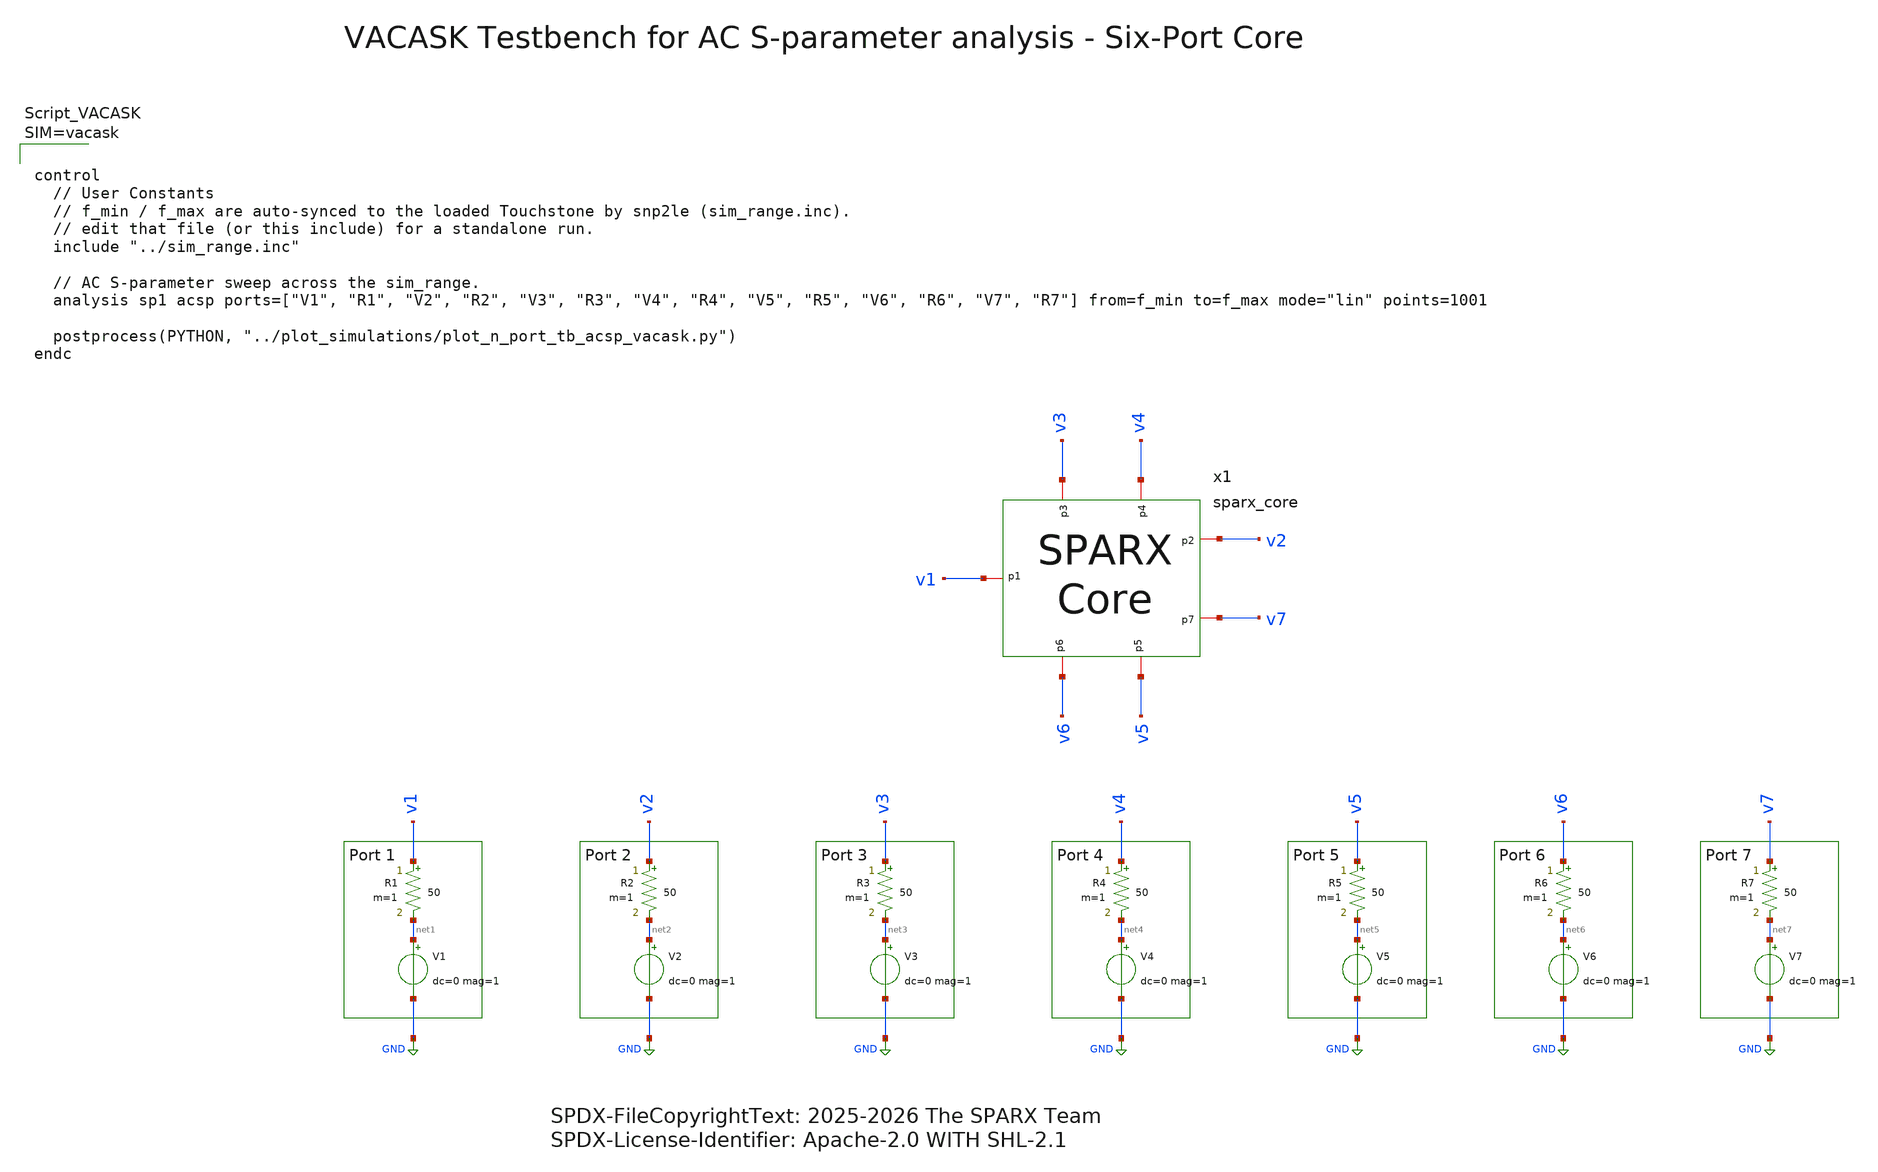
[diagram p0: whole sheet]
** sch_path: testbenches/xschem/sparx_core_tb_acsp_vacask.sch
* SPDX-FileCopyrightText: 2025-2026 The SPARX Team
* SPDX-License-Identifier: Apache-2.0 WITH SHL-2.1
**.subckt sparx_core_tb_acsp_vacask
R1 v1 net1 50 m=1
V1 net1 GND dc=0 mag=1
R2 v2 net2 50 m=1
V2 net2 GND dc=0 mag=1
R3 v3 net3 50 m=1
V3 net3 GND dc=0 mag=1
R4 v4 net4 50 m=1
V4 net4 GND dc=0 mag=1
R5 v5 net5 50 m=1
V5 net5 GND dc=0 mag=1
R6 v6 net6 50 m=1
V6 net6 GND dc=0 mag=1
R7 v7 net7 50 m=1
V7 net7 GND dc=0 mag=1
x1 v3 v4 v2 v1 v7 v5 v6 sparx_core
**** begin user architecture code






**** end user architecture code
**.ends

* expanding   symbol:  sparx_core.sym # of pins=7
** sym_path: schematic/sparx_core.sym
** sch_path: schematic/sparx_core.sch
.subckt sparx_core p3 p4 p2 p1 p7 p5 p6
*.iopin p1
*.iopin p3
*.iopin p4
*.iopin p2
*.iopin p7
*.iopin p6
*.iopin p5
x5 net3 net1 p4 p3 sparx_blc_le
x6 p2 p7 net2 net1 sparx_blc_le
x7 net5 net4 net3 sparx_wpd_le
x8 p1 net5 sparx_bpf_le
x4 net4 net2 p5 p6 sparx_blc_le
.ends

.GLOBAL GND
.end
